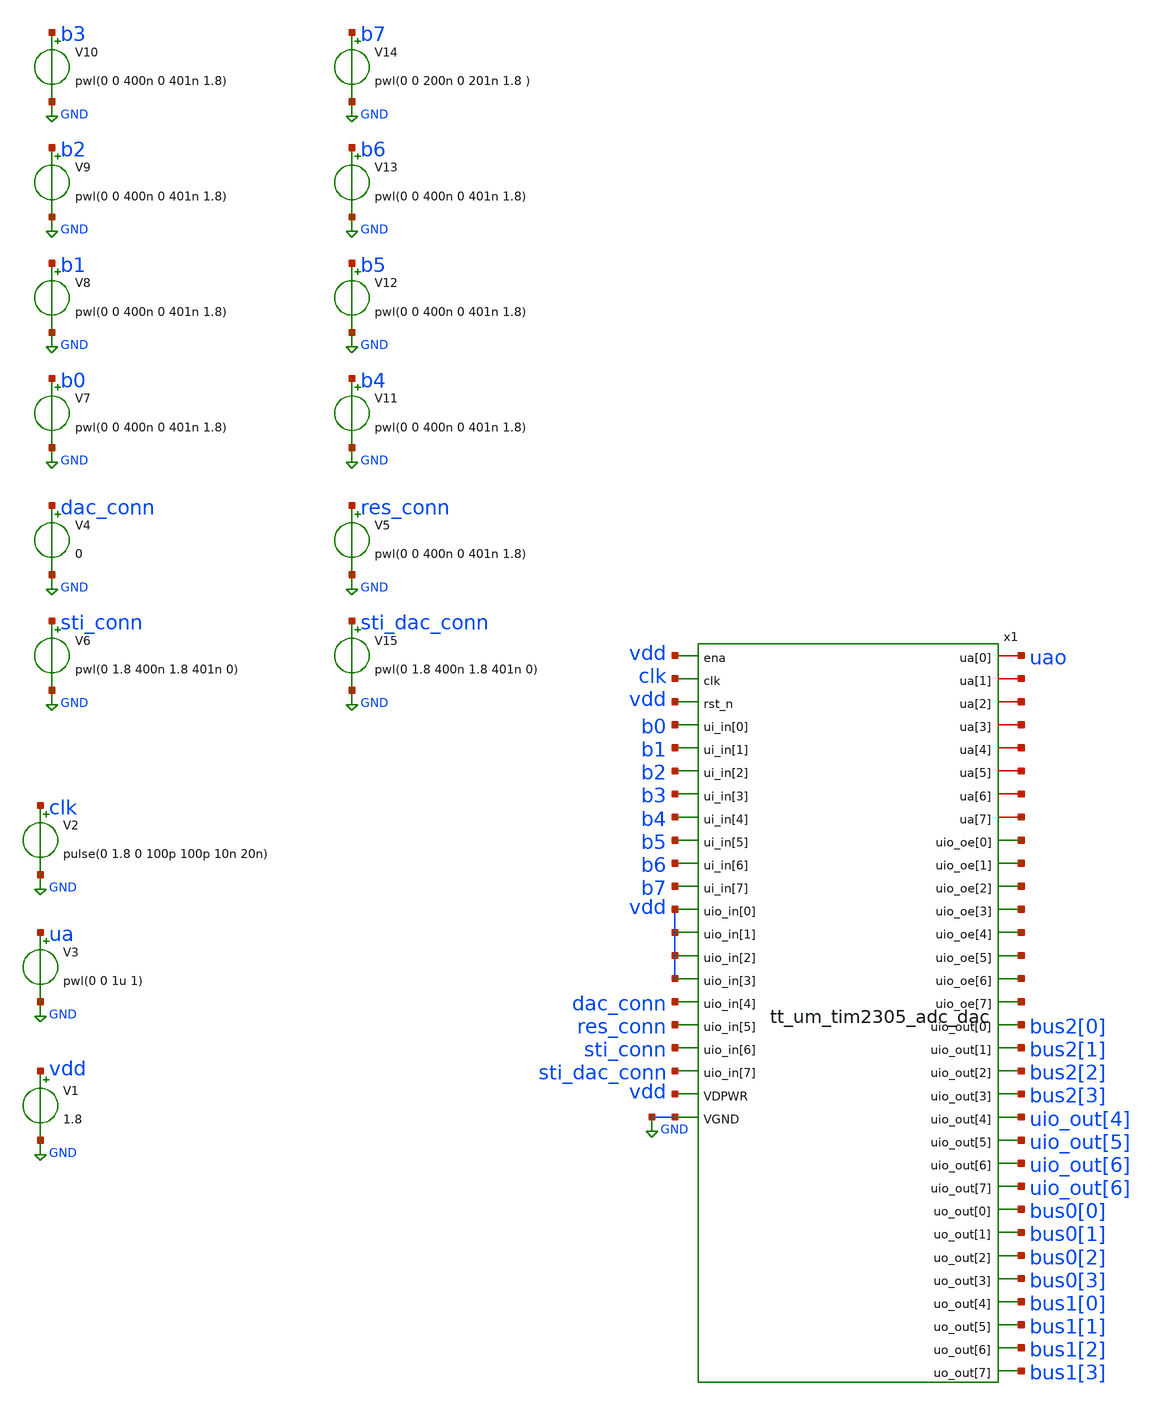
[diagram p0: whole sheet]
** sch_path: xschem/top_tb.sch
**.subckt top_tb
V1 vdd GND 1.8
V3 ua GND pwl(0 0 1u 1)
V2 clk GND pulse(0 1.8 0 100p 100p 10n 20n)
x1 uao net1 net2 net3 net4 net5 net6 vdd net7 clk vdd net8 b0 net9 b1 net10 net11 b2 b3 net12 b4
+ net13 b5 net14 net15 b6 b7 bus2[0] vdd bus2[1] vdd bus2[2] vdd bus2[3] uio_out[4] vdd uio_out[5] dac_conn
+ uio_out[6] res_conn sti_conn uio_out[6] sti_dac_conn bus0[0] vdd bus0[1] GND bus0[2] bus0[3] bus1[0] bus1[1]
+ bus1[2] bus1[3] tt_um_tim2305_adc_dac
V7 b0 GND pwl(0 0 400n 0 401n 1.8)
V8 b1 GND pwl(0 0 400n 0 401n 1.8)
V9 b2 GND pwl(0 0 400n 0 401n 1.8)
V10 b3 GND pwl(0 0 400n 0 401n 1.8)
V11 b4 GND pwl(0 0 400n 0 401n 1.8)
V12 b5 GND pwl(0 0 400n 0 401n 1.8)
V13 b6 GND pwl(0 0 400n 0 401n 1.8)
V14 b7 GND pwl(0 0 200n 0 201n 1.8 )
V4 dac_conn GND 0
V5 res_conn GND pwl(0 0 400n 0 401n 1.8)
V6 sti_conn GND pwl(0 1.8 400n 1.8 401n 0)
V15 sti_dac_conn GND pwl(0 1.8 400n 1.8 401n 0)
**** begin user architecture code


.tran 100p 500n
.save all
.lib /home/ttuser/pdk/sky130A/libs.tech/ngspice/sky130.lib.spice tt
.include /home/ttuser/Documents/github_project/adc_dac2/mag/tt_um_tim2305_adc_dac.spice


**** end user architecture code
**.ends
.GLOBAL GND
.end
